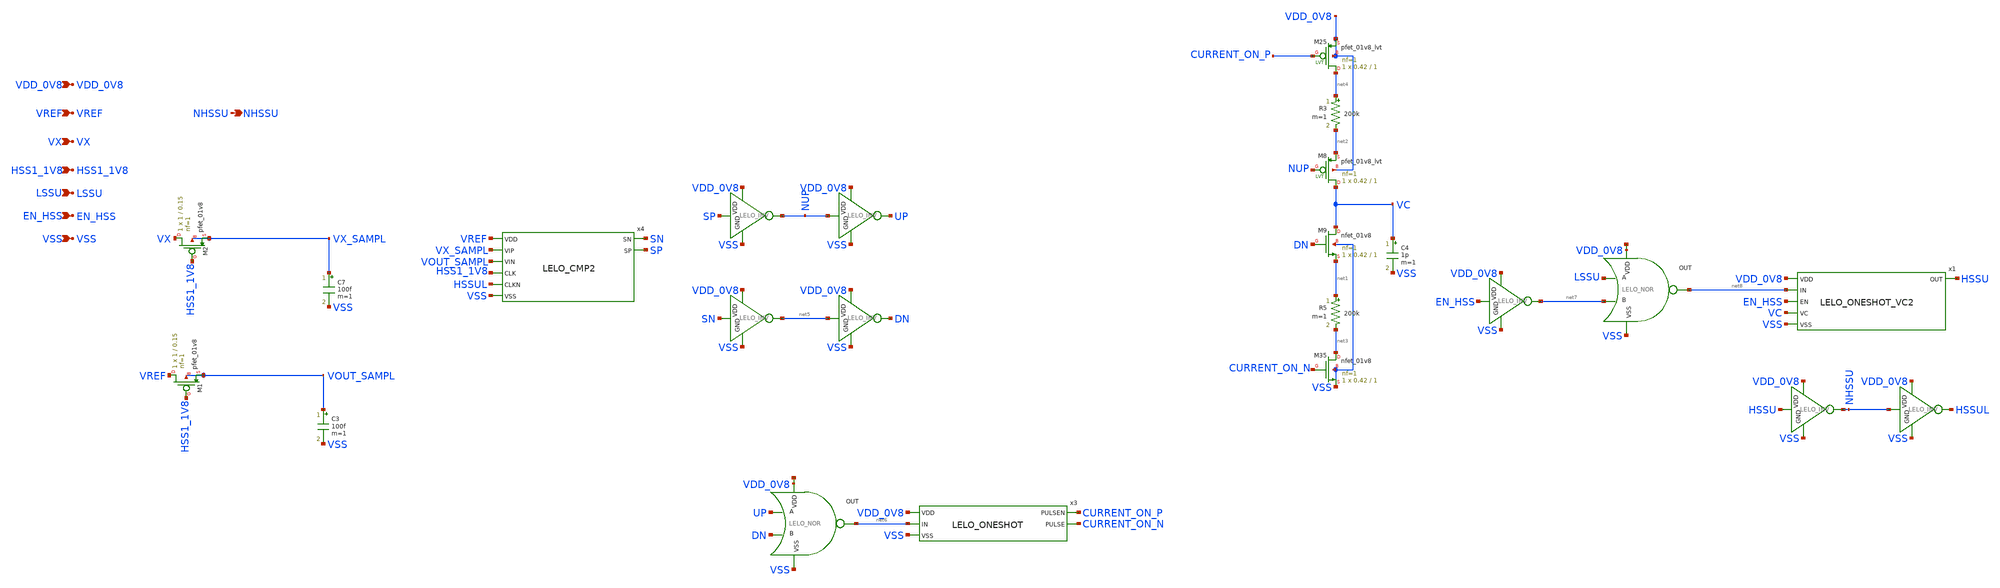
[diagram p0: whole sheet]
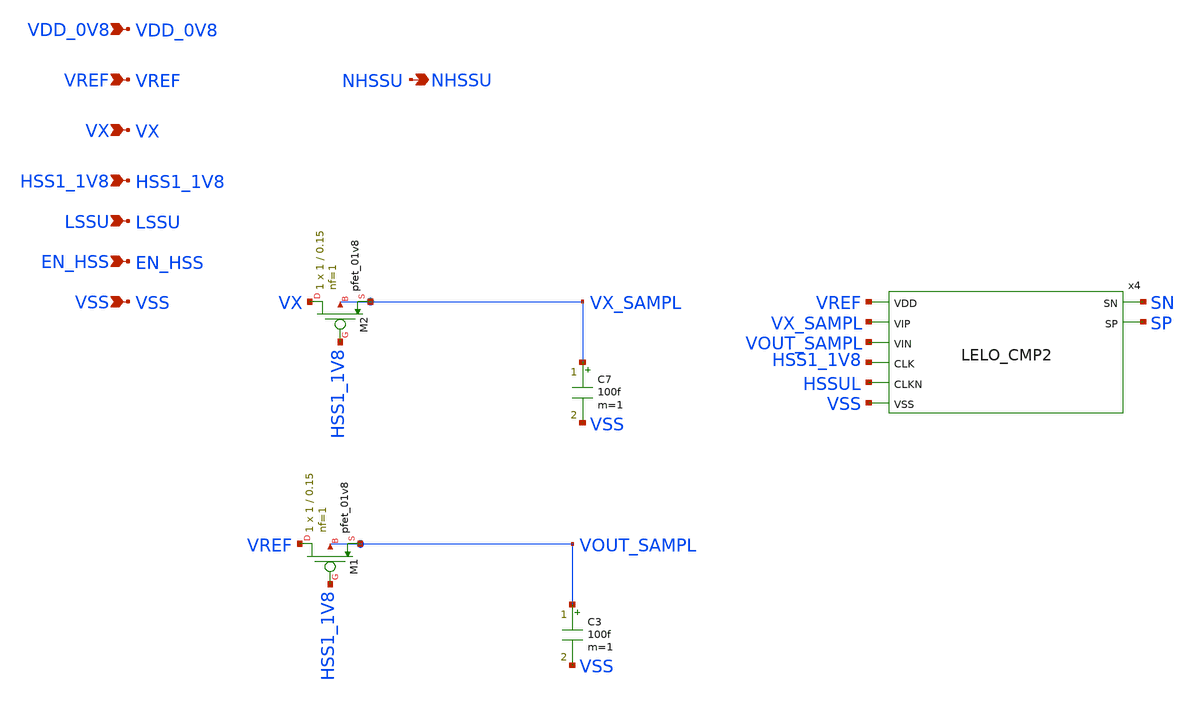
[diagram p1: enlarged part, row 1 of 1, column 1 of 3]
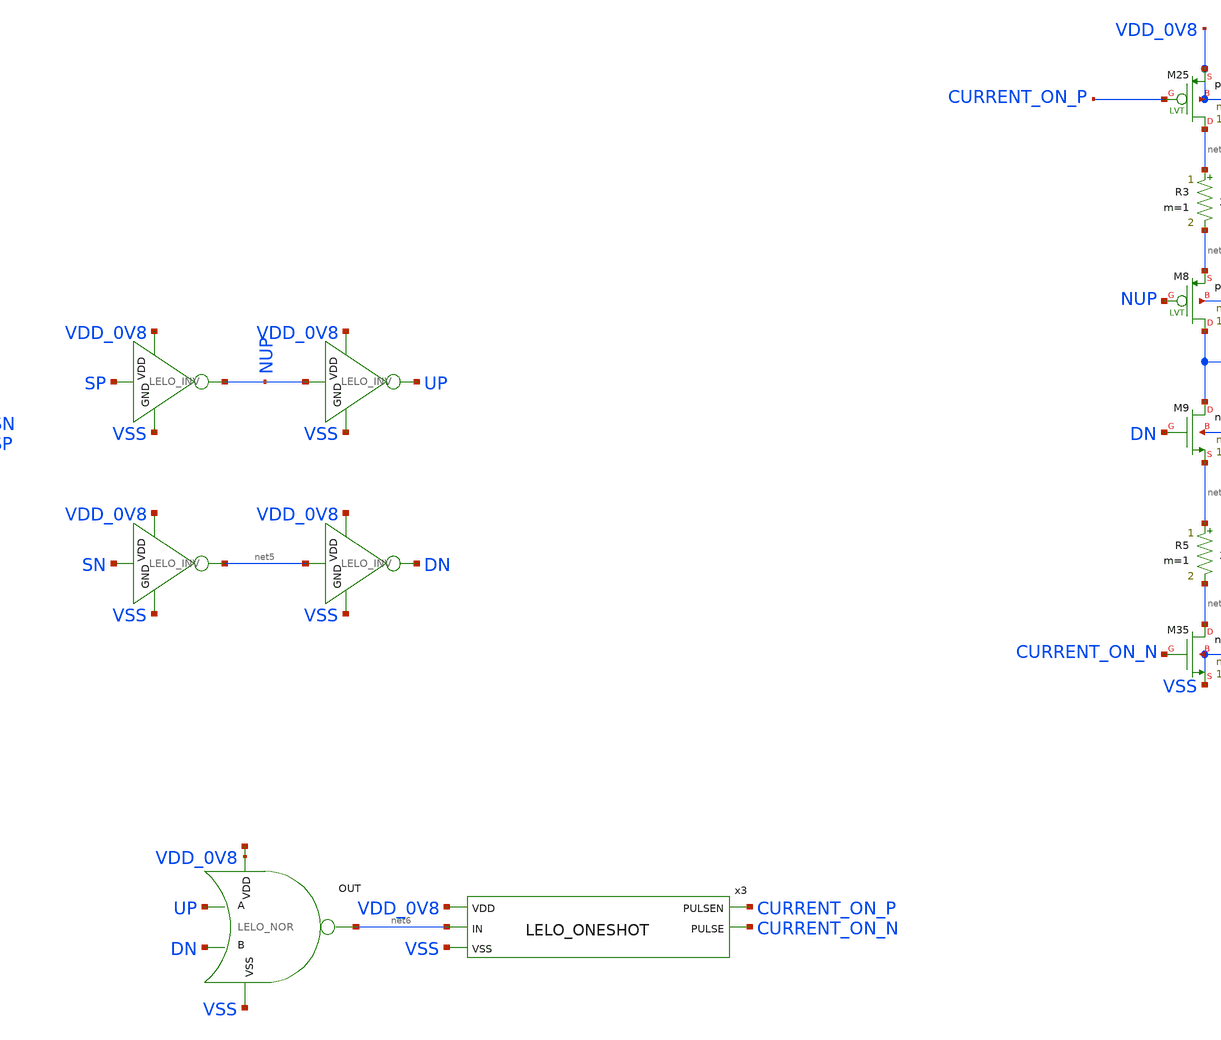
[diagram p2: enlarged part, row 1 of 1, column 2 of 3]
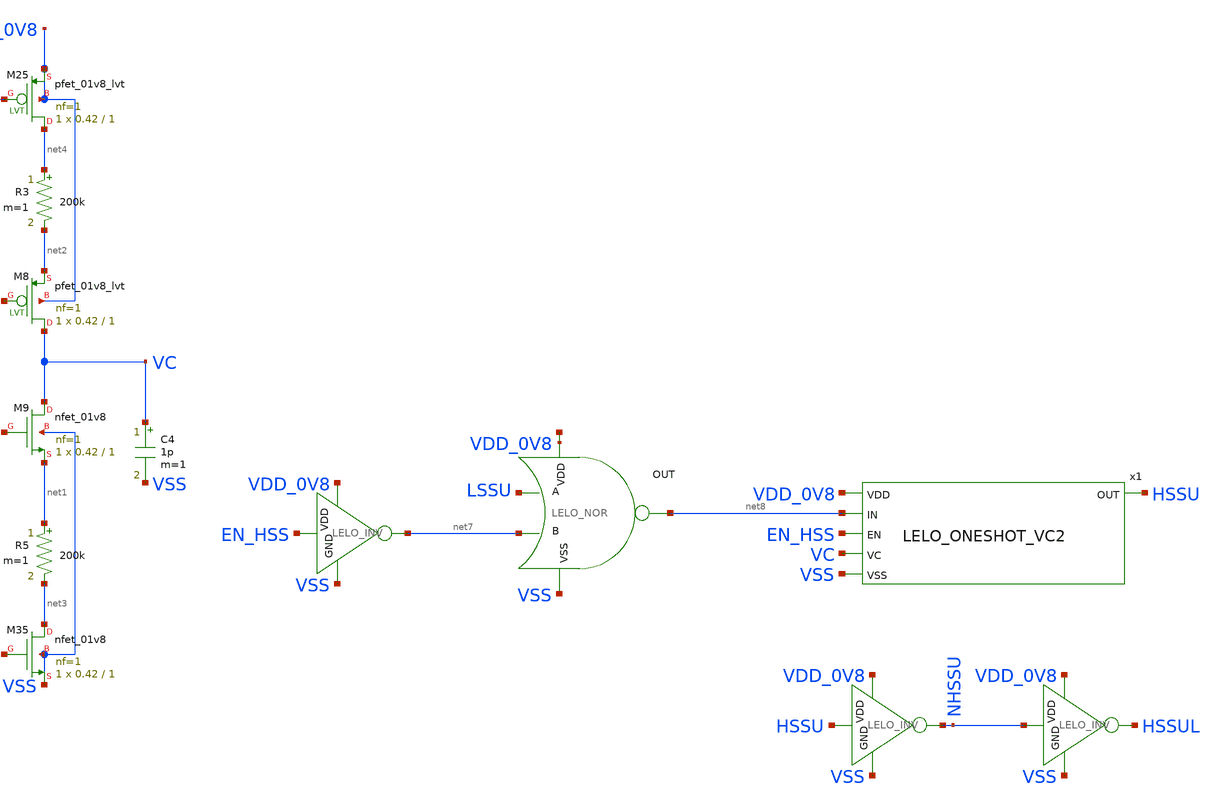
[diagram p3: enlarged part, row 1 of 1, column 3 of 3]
** sch_path: design/LELO_SVOD_SKY130A/LELO_SVOD_HSSCNTRL2.sch
**.subckt LELO_SVOD_HSSCNTRL2 VREF NHSSU VX LSSU VSS EN_HSS VDD_0V8 HSS1_1V8
*.ipin VREF
*.opin NHSSU
*.ipin VX
*.ipin LSSU
*.ipin VSS
*.ipin EN_HSS
*.ipin VDD_0V8
*.ipin HSS1_1V8
C7 VX_SAMPL VSS 100f m=1
C3 VOUT_SAMPL VSS 100f m=1
C4 VC VSS 1p m=1
XM9 VC DN net1 VSS sky130_fd_pr__nfet_01v8 L=1 W=0.42 nf=1 ad='int((1 + 1)/2) * 0.42 / 1 * 0.29' as='int((1 + 2)/2) * 0.42 / 1 * 0.29'
+ pd='2*int((1 + 1)/2) * (0.42 / 1 + 0.29)' ps='2*int((1 + 2)/2) * (0.42 / 1 + 0.29)' nrd='0.29 / 0.42 '
+ nrs='0.29 / 0.42 ' sa=0 sb=0 sd=0 mult=1 m=1
x10 VDD_0V8 SP NUP VSS LELO_INV
R5 net1 net3 200k m=1
XM35 net3 CURRENT_ON_N VSS VSS sky130_fd_pr__nfet_01v8 L=1 W=0.42 nf=1 ad='int((1 + 1)/2) * 0.42 / 1 * 0.29'
+ as='int((1 + 2)/2) * 0.42 / 1 * 0.29' pd='2*int((1 + 1)/2) * (0.42 / 1 + 0.29)' ps='2*int((1 + 2)/2) * (0.42 / 1 + 0.29)'
+ nrd='0.29 / 0.42 ' nrs='0.29 / 0.42 ' sa=0 sb=0 sd=0 mult=1 m=1
x11 VDD_0V8 SN net5 VSS LELO_INV
x14 VDD_0V8 net5 DN VSS LELO_INV
x17 VDD_0V8 NUP UP VSS LELO_INV
x2 net9 net6 UP DN VSS LELO_NOR
x3 VDD_0V8 net6 VSS CURRENT_ON_P CURRENT_ON_N LELO_ONESHOT
R3 net4 net2 200k m=1
XM8 VC NUP net2 VDD_0V8 sky130_fd_pr__pfet_01v8_lvt L=1 W=0.42 nf=1 ad='int((1 + 1)/2) * 0.42 / 1 * 0.29'
+ as='int((1 + 2)/2) * 0.42 / 1 * 0.29' pd='2*int((1 + 1)/2) * (0.42 / 1 + 0.29)' ps='2*int((1 + 2)/2) * (0.42 / 1 + 0.29)'
+ nrd='0.29 / 0.42 ' nrs='0.29 / 0.42 ' sa=0 sb=0 sd=0 mult=1 m=1
XM25 net4 CURRENT_ON_P VDD_0V8 VDD_0V8 sky130_fd_pr__pfet_01v8_lvt L=1 W=0.42 nf=1 ad='int((1 + 1)/2) * 0.42 / 1 * 0.29'
+ as='int((1 + 2)/2) * 0.42 / 1 * 0.29' pd='2*int((1 + 1)/2) * (0.42 / 1 + 0.29)' ps='2*int((1 + 2)/2) * (0.42 / 1 + 0.29)'
+ nrd='0.29 / 0.42 ' nrs='0.29 / 0.42 ' sa=0 sb=0 sd=0 mult=1 m=1
x1 VDD_0V8 net8 EN_HSS HSSU VC VSS LELO_ONESHOT_VC2
x5 net10 net8 LSSU net7 VSS LELO_NOR
x6 VDD_0V8 EN_HSS net7 VSS LELO_INV
x7 VDD_0V8 HSSU NHSSU VSS LELO_INV
x8 VDD_0V8 NHSSU HSSUL VSS LELO_INV
XM1 VREF HSS1_1V8 VOUT_SAMPL VOUT_SAMPL sky130_fd_pr__pfet_01v8 L=0.15 W=1 nf=1 ad='int((1 + 1)/2) * 1 / 1 * 0.29'
+ as='int((1 + 2)/2) * 1 / 1 * 0.29' pd='2*int((1 + 1)/2) * (1 / 1 + 0.29)' ps='2*int((1 + 2)/2) * (1 / 1 + 0.29)'
+ nrd='0.29 / 1 ' nrs='0.29 / 1 ' sa=0 sb=0 sd=0 mult=1 m=1
XM2 VX HSS1_1V8 VX_SAMPL VX_SAMPL sky130_fd_pr__pfet_01v8 L=0.15 W=1 nf=1 ad='int((1 + 1)/2) * 1 / 1 * 0.29'
+ as='int((1 + 2)/2) * 1 / 1 * 0.29' pd='2*int((1 + 1)/2) * (1 / 1 + 0.29)' ps='2*int((1 + 2)/2) * (1 / 1 + 0.29)'
+ nrd='0.29 / 1 ' nrs='0.29 / 1 ' sa=0 sb=0 sd=0 mult=1 m=1
x4 SN SP VREF VX_SAMPL VOUT_SAMPL HSS1_1V8 HSSUL VSS LELO_CMP2
**.ends
.end
